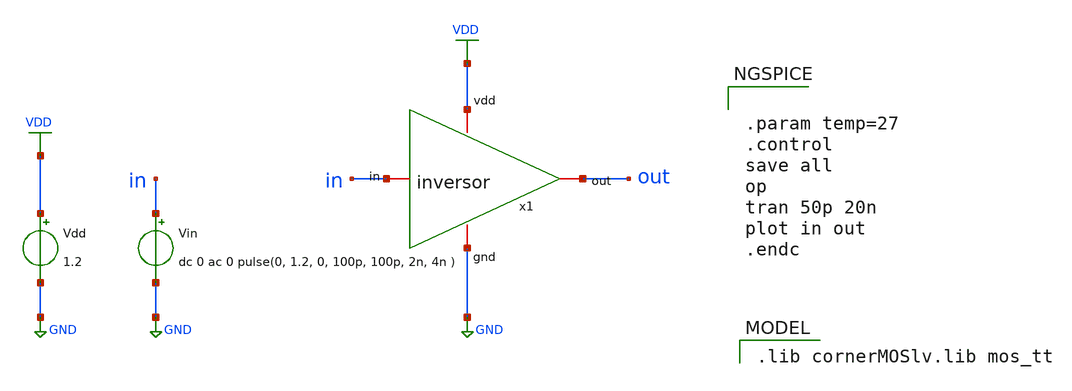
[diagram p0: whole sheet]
** sch_path: tb-inversor-tran.sch
**.subckt tb-inversor-tran
x1 VDD out in GND inversor
Vdd VDD GND 1.2
Vin in GND dc 0 ac 0 pulse(0, 1.2, 0, 100p, 100p, 2n, 4n )
**** begin user architecture code


.param temp=27
.control
save all
op
tran 50p 20n
plot in out
.endc


 .lib cornerMOSlv.lib mos_tt

**** end user architecture code
**.ends
.GLOBAL GND
.GLOBAL VDD
.end
